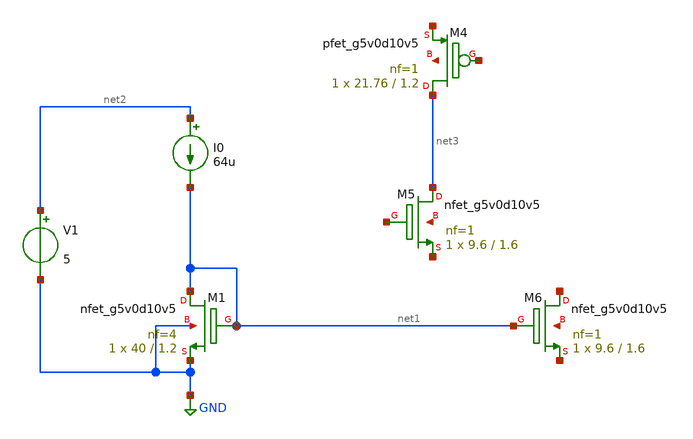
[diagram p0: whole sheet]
** sch_path: untitled-1.sch
**.subckt untitled-1
XM1 net1 net1 GND GND sky130_fd_pr__nfet_g5v0d10v5 L=1.2 W=40 nf=4 ad='int((nf+1)/2) * W/nf * 0.29' as='int((nf+2)/2) * W/nf * 0.29'
+ pd='2*int((nf+1)/2) * (W/nf + 0.29)' ps='2*int((nf+2)/2) * (W/nf + 0.29)' nrd='0.29 / W' nrs='0.29 / W'
+ sa=0 sb=0 sd=0 mult=1 m=1
I0 net2 net1 64u
V1 net2 GND 5
XM4 net3 net4 net5 net6 sky130_fd_pr__pfet_g5v0d10v5 L=1.2 W=21.76 nf=1 ad='int((nf+1)/2) * W/nf * 0.29'
+ as='int((nf+2)/2) * W/nf * 0.29' pd='2*int((nf+1)/2) * (W/nf + 0.29)' ps='2*int((nf+2)/2) * (W/nf + 0.29)'
+ nrd='0.29 / W' nrs='0.29 / W' sa=0 sb=0 sd=0 mult=1 m=1
XM5 net3 net7 net8 net9 sky130_fd_pr__nfet_g5v0d10v5 L=1.6 W=9.6 nf=1 ad='int((nf+1)/2) * W/nf * 0.29'
+ as='int((nf+2)/2) * W/nf * 0.29' pd='2*int((nf+1)/2) * (W/nf + 0.29)' ps='2*int((nf+2)/2) * (W/nf + 0.29)'
+ nrd='0.29 / W' nrs='0.29 / W' sa=0 sb=0 sd=0 mult=1 m=1
XM6 net10 net1 net11 net12 sky130_fd_pr__nfet_g5v0d10v5 L=1.6 W=9.6 nf=1 ad='int((nf+1)/2) * W/nf * 0.29'
+ as='int((nf+2)/2) * W/nf * 0.29' pd='2*int((nf+1)/2) * (W/nf + 0.29)' ps='2*int((nf+2)/2) * (W/nf + 0.29)'
+ nrd='0.29 / W' nrs='0.29 / W' sa=0 sb=0 sd=0 mult=1 m=1
**.ends
.GLOBAL GND
.end
